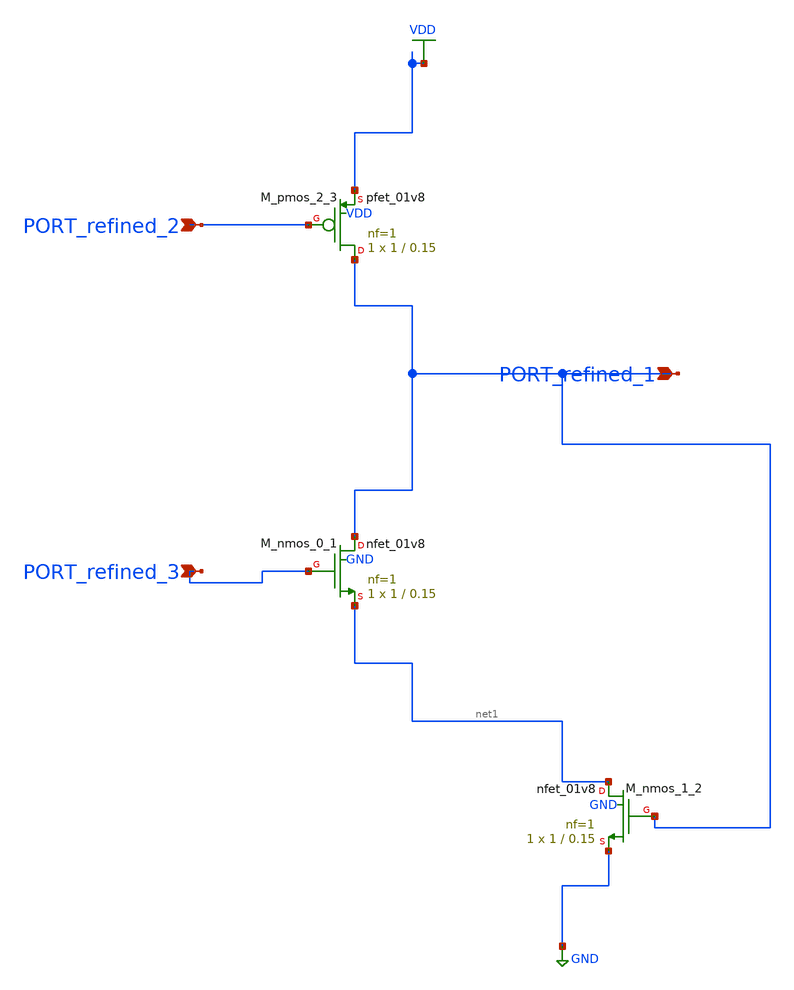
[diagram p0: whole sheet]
** sch_path: schematics/AMSNet/677.sch
**.subckt 677 PORT_refined_2 PORT_refined_1 PORT_refined_3
*.ipin PORT_refined_2
*.ipin PORT_refined_1
*.ipin PORT_refined_3
XM_nmos_0_1 PORT_refined_1 PORT_refined_3 net1 GND sky130_fd_pr__nfet_01v8 L=0.15 W=1 nf=1 ad='int((1 + 1)/2) * 1 / 1 * 0.29'
+ as='int((1 + 2)/2) * 1 / 1 * 0.29' pd='2*int((1 + 1)/2) * (1 / 1 + 0.29)' ps='2*int((1 + 2)/2) * (1 / 1 + 0.29)'
+ nrd='0.29 / 1 ' nrs='0.29 / 1 ' sa=0 sb=0 sd=0 mult=1 m=1
XM_nmos_1_2 net1 PORT_refined_1 GND GND sky130_fd_pr__nfet_01v8 L=0.15 W=1 nf=1 ad='int((1 + 1)/2) * 1 / 1 * 0.29'
+ as='int((1 + 2)/2) * 1 / 1 * 0.29' pd='2*int((1 + 1)/2) * (1 / 1 + 0.29)' ps='2*int((1 + 2)/2) * (1 / 1 + 0.29)'
+ nrd='0.29 / 1 ' nrs='0.29 / 1 ' sa=0 sb=0 sd=0 mult=1 m=1
XM_pmos_2_3 PORT_refined_1 PORT_refined_2 VDD VDD sky130_fd_pr__pfet_01v8 L=0.15 W=1 nf=1 ad='int((1 + 1)/2) * 1 / 1 * 0.29'
+ as='int((1 + 2)/2) * 1 / 1 * 0.29' pd='2*int((1 + 1)/2) * (1 / 1 + 0.29)' ps='2*int((1 + 2)/2) * (1 / 1 + 0.29)'
+ nrd='0.29 / 1 ' nrs='0.29 / 1 ' sa=0 sb=0 sd=0 mult=1 m=1
**.ends
.GLOBAL GND
.GLOBAL VDD
.end
